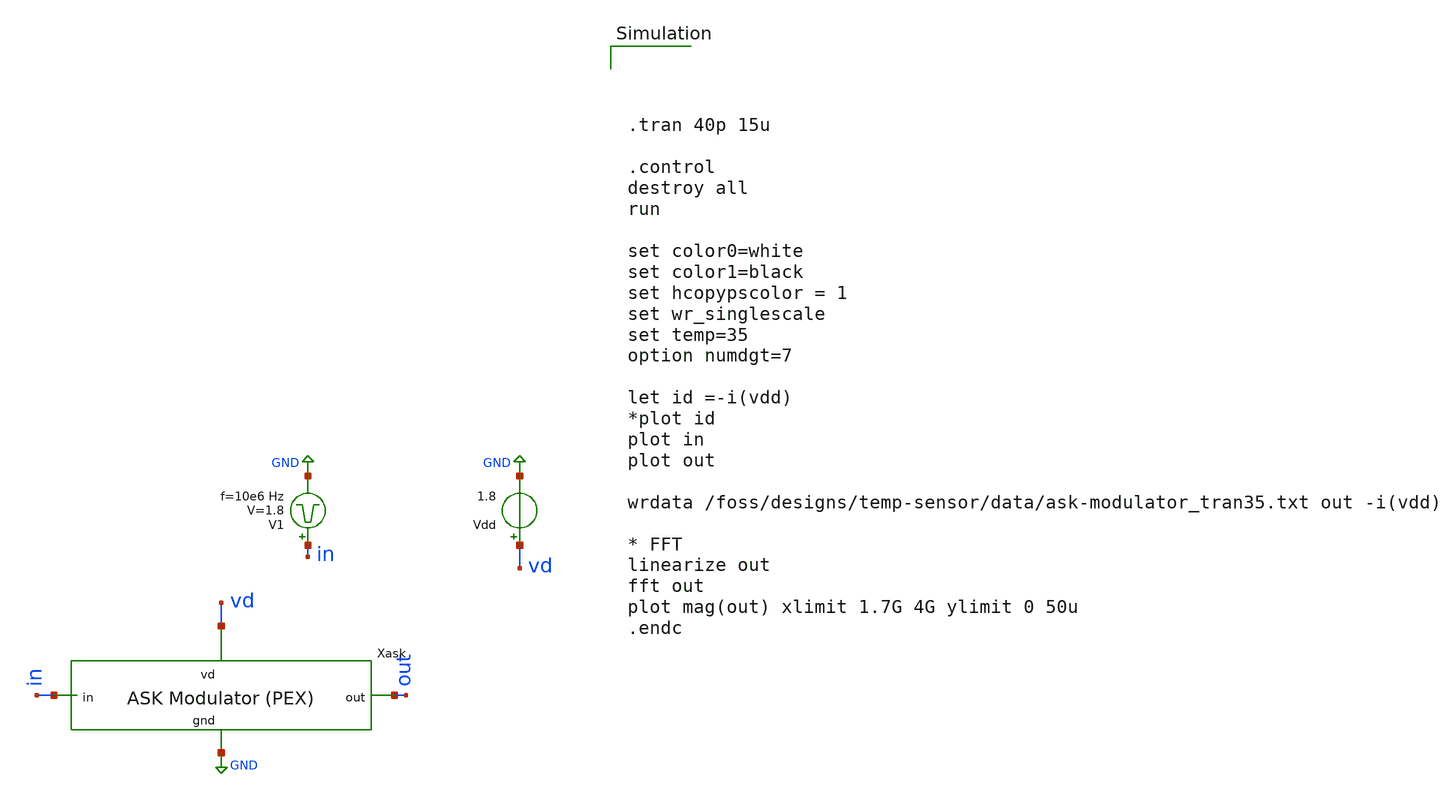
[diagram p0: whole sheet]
** sch_path: ask_modulator/xschem/ask-modulator_tb-tran.sch
**.subckt ask-modulator_tb-tran
Vdd vd GND 1.8
V1 in GND pulse 0 1.8 '0.495/ 10e6 ' '0.01/10e6 ' '0.01/10e6 ' '0.49/10e6 ' '1/10e6 '
x1 vd out in GND ask-modulator-pex
**** begin user architecture code




.tran 40p 15u

.control
destroy all
run

set color0=white
set color1=black
set hcopypscolor = 1
set wr_singlescale
set temp=35
option numdgt=7

let id =-i(vdd)
*plot id
plot in
plot out

wrdata /foss/designs/temp-sensor/data/ask-modulator_tran35.txt out -i(vdd)

* FFT
linearize out
fft out
plot mag(out) xlimit 1.7G 4G ylimit 0 50u
.endc

 .lib $::SKYWATER_MODELS/sky130.lib.spice tt
.include $::SKYWATER_STDCELLS/sky130_fd_sc_hd.spice

**** end user architecture code
**.ends
.GLOBAL GND
.end
